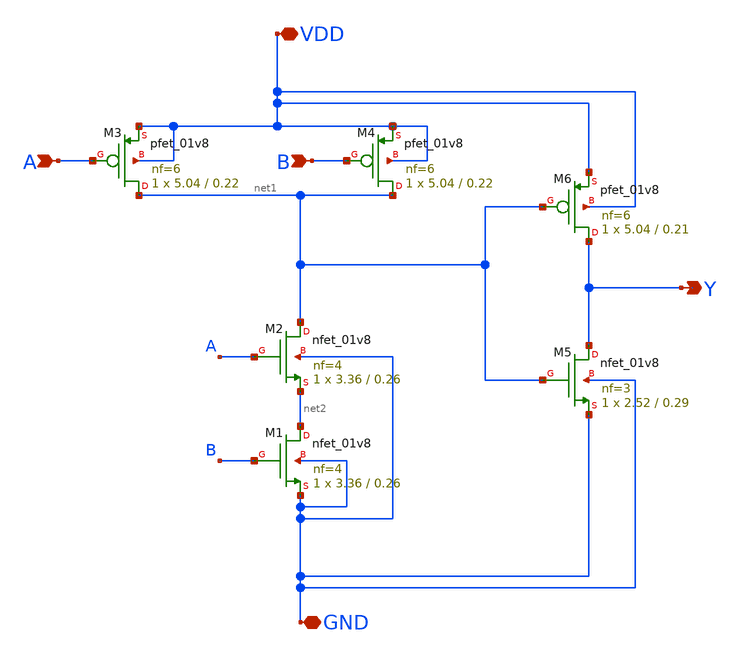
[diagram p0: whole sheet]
** sch_path: cells/AND2X4/schematic/and2x4.sch
**.subckt and2x4 A B VDD GND Y
*.ipin A
*.ipin B
*.iopin VDD
*.iopin GND
*.opin Y
XM2 net1 A net2 GND sky130_fd_pr__nfet_01v8 L=0.26 W=3.36 nf=4 ad='int((4 + 1)/2) * 3.36 / 4 * 0.29'
+ as='int((4 + 2)/2) * 3.36 / 4 * 0.29' pd='2*int((4 + 1)/2) * (3.36 / 4 + 0.29)' ps='2*int((4 + 2)/2) * (3.36 / 4 + 0.29)'
+ nrd='0.29 / 3.36 ' nrs='0.29 / 3.36 ' sa=0 sb=0 sd=0 mult=1 m=1
XM3 net1 A VDD VDD sky130_fd_pr__pfet_01v8 L=0.22 W=5.04 nf=6 ad='int((6 + 1)/2) * 5.04 / 6 * 0.29' as='int((6 + 2)/2) * 5.04 / 6 * 0.29'
+ pd='2*int((6 + 1)/2) * (5.04 / 6 + 0.29)' ps='2*int((6 + 2)/2) * (5.04 / 6 + 0.29)' nrd='0.29 / 5.04 '
+ nrs='0.29 / 5.04 ' sa=0 sb=0 sd=0 mult=1 m=1
XM5 Y net1 GND GND sky130_fd_pr__nfet_01v8 L=0.29 W=2.52 nf=3 ad='int((3 + 1)/2) * 2.52 / 3 * 0.29' as='int((3 + 2)/2) * 2.52 / 3 * 0.29'
+ pd='2*int((3 + 1)/2) * (2.52 / 3 + 0.29)' ps='2*int((3 + 2)/2) * (2.52 / 3 + 0.29)' nrd='0.29 / 2.52 '
+ nrs='0.29 / 2.52 ' sa=0 sb=0 sd=0 mult=1 m=1
XM4 net1 B VDD VDD sky130_fd_pr__pfet_01v8 L=0.22 W=5.04 nf=6 ad='int((6 + 1)/2) * 5.04 / 6 * 0.29' as='int((6 + 2)/2) * 5.04 / 6 * 0.29'
+ pd='2*int((6 + 1)/2) * (5.04 / 6 + 0.29)' ps='2*int((6 + 2)/2) * (5.04 / 6 + 0.29)' nrd='0.29 / 5.04 '
+ nrs='0.29 / 5.04 ' sa=0 sb=0 sd=0 mult=1 m=1
XM6 Y net1 VDD VDD sky130_fd_pr__pfet_01v8 L=0.21 W=5.04 nf=6 ad='int((6 + 1)/2) * 5.04 / 6 * 0.29' as='int((6 + 2)/2) * 5.04 / 6 * 0.29'
+ pd='2*int((6 + 1)/2) * (5.04 / 6 + 0.29)' ps='2*int((6 + 2)/2) * (5.04 / 6 + 0.29)' nrd='0.29 / 5.04 '
+ nrs='0.29 / 5.04 ' sa=0 sb=0 sd=0 mult=1 m=1
XM1 net2 B GND GND sky130_fd_pr__nfet_01v8 L=0.26 W=3.36 nf=4 ad='int((4 + 1)/2) * 3.36 / 4 * 0.29' as='int((4 + 2)/2) * 3.36 / 4 * 0.29'
+ pd='2*int((4 + 1)/2) * (3.36 / 4 + 0.29)' ps='2*int((4 + 2)/2) * (3.36 / 4 + 0.29)' nrd='0.29 / 3.36 '
+ nrs='0.29 / 3.36 ' sa=0 sb=0 sd=0 mult=1 m=1
**.ends
.end
